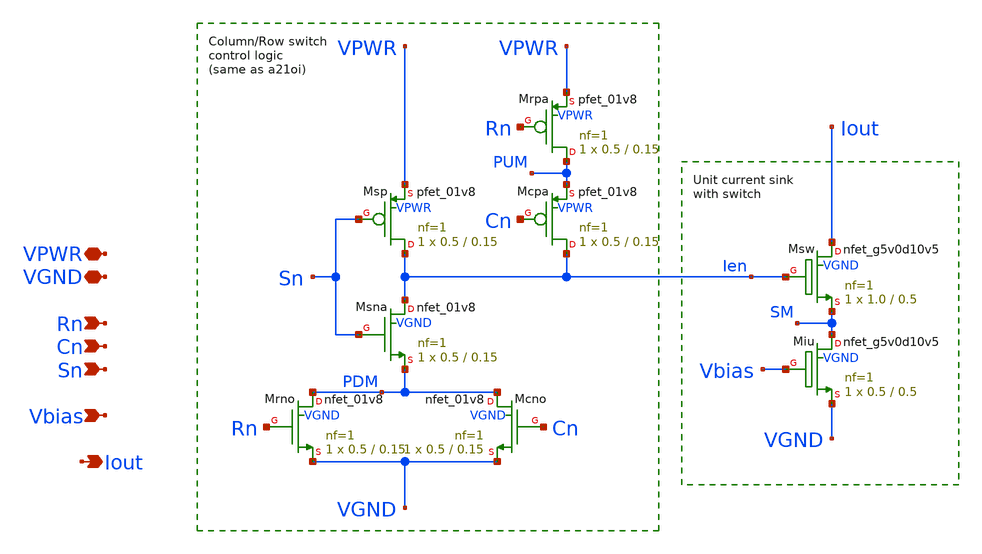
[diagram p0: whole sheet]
** sch_path: xschem/icell.sch
**.subckt icell Rn VPWR Iout VGND Cn Sn Vbias
*.ipin Rn
*.iopin VPWR
*.opin Iout
*.iopin VGND
*.ipin Cn
*.ipin Sn
*.ipin Vbias
XMsp Ien Sn VPWR VPWR sky130_fd_pr__pfet_01v8 L=0.15 W=0.5 nf=1 ad='int((nf+1)/2) * W/nf * 0.29' as='int((nf+2)/2) * W/nf * 0.29'
+ pd='2*int((nf+1)/2) * (W/nf + 0.29)' ps='2*int((nf+2)/2) * (W/nf + 0.29)' nrd='0.29 / W' nrs='0.29 / W'
+ sa=0 sb=0 sd=0 mult=1 m=1
XMsna Ien Sn PDM VGND sky130_fd_pr__nfet_01v8 L=0.15 W=0.5 nf=1 ad='int((nf+1)/2) * W/nf * 0.29' as='int((nf+2)/2) * W/nf * 0.29'
+ pd='2*int((nf+1)/2) * (W/nf + 0.29)' ps='2*int((nf+2)/2) * (W/nf + 0.29)' nrd='0.29 / W' nrs='0.29 / W'
+ sa=0 sb=0 sd=0 mult=1 m=1
XMcpa Ien Cn PUM VPWR sky130_fd_pr__pfet_01v8 L=0.15 W=0.5 nf=1 ad='int((nf+1)/2) * W/nf * 0.29' as='int((nf+2)/2) * W/nf * 0.29'
+ pd='2*int((nf+1)/2) * (W/nf + 0.29)' ps='2*int((nf+2)/2) * (W/nf + 0.29)' nrd='0.29 / W' nrs='0.29 / W'
+ sa=0 sb=0 sd=0 mult=1 m=1
XMrpa PUM Rn VPWR VPWR sky130_fd_pr__pfet_01v8 L=0.15 W=0.5 nf=1 ad='int((nf+1)/2) * W/nf * 0.29' as='int((nf+2)/2) * W/nf * 0.29'
+ pd='2*int((nf+1)/2) * (W/nf + 0.29)' ps='2*int((nf+2)/2) * (W/nf + 0.29)' nrd='0.29 / W' nrs='0.29 / W'
+ sa=0 sb=0 sd=0 mult=1 m=1
XMrno PDM Rn VGND VGND sky130_fd_pr__nfet_01v8 L=0.15 W=0.5 nf=1 ad='int((nf+1)/2) * W/nf * 0.29' as='int((nf+2)/2) * W/nf * 0.29'
+ pd='2*int((nf+1)/2) * (W/nf + 0.29)' ps='2*int((nf+2)/2) * (W/nf + 0.29)' nrd='0.29 / W' nrs='0.29 / W'
+ sa=0 sb=0 sd=0 mult=1 m=1
XMcno PDM Cn VGND VGND sky130_fd_pr__nfet_01v8 L=0.15 W=0.5 nf=1 ad='int((nf+1)/2) * W/nf * 0.29' as='int((nf+2)/2) * W/nf * 0.29'
+ pd='2*int((nf+1)/2) * (W/nf + 0.29)' ps='2*int((nf+2)/2) * (W/nf + 0.29)' nrd='0.29 / W' nrs='0.29 / W'
+ sa=0 sb=0 sd=0 mult=1 m=1
XMiu SM Vbias VGND VGND sky130_fd_pr__nfet_g5v0d10v5 L=0.5 W=0.5 nf=1 ad='int((nf+1)/2) * W/nf * 0.29'
+ as='int((nf+2)/2) * W/nf * 0.29' pd='2*int((nf+1)/2) * (W/nf + 0.29)' ps='2*int((nf+2)/2) * (W/nf + 0.29)'
+ nrd='0.29 / W' nrs='0.29 / W' sa=0 sb=0 sd=0 mult=1 m=1
XMsw Iout Ien SM VGND sky130_fd_pr__nfet_g5v0d10v5 L=0.5 W=1.0 nf=1 ad='int((nf+1)/2) * W/nf * 0.29'
+ as='int((nf+2)/2) * W/nf * 0.29' pd='2*int((nf+1)/2) * (W/nf + 0.29)' ps='2*int((nf+2)/2) * (W/nf + 0.29)'
+ nrd='0.29 / W' nrs='0.29 / W' sa=0 sb=0 sd=0 mult=1 m=1
**.ends
.end
